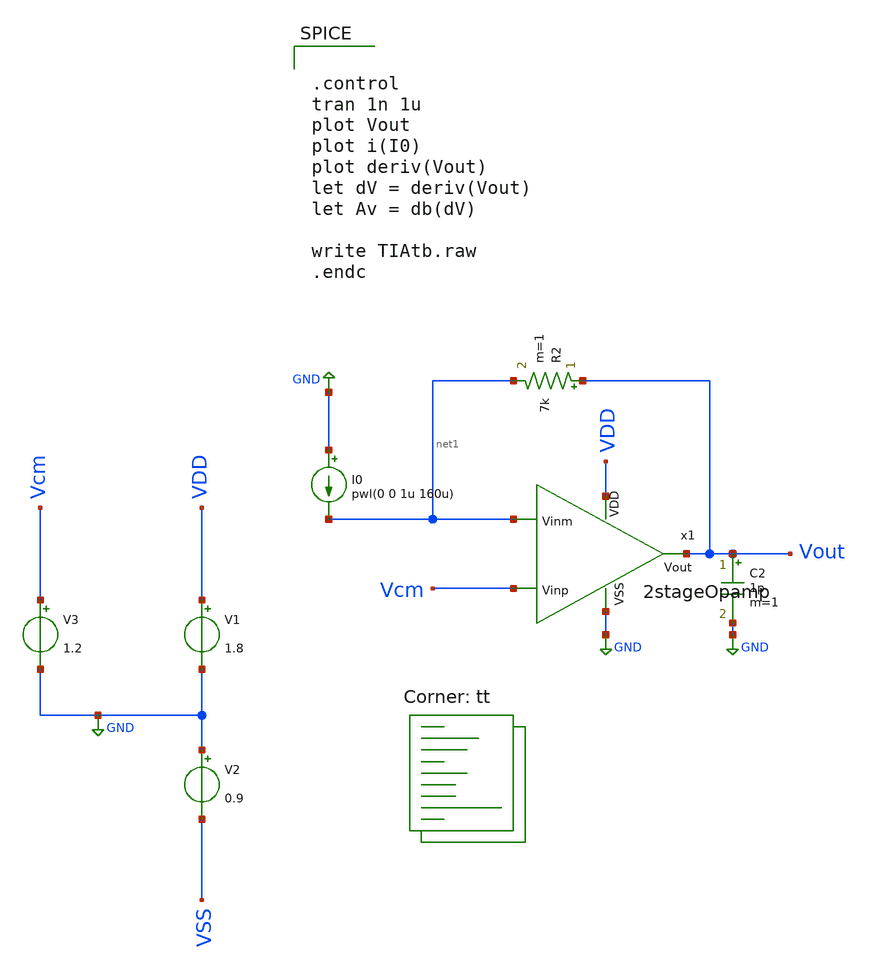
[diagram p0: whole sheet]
** sch_path: xschem/TestBenches/TIAtb.sch
**.subckt TIAtb
C2 Vout GND 1p m=1
x1 VDD net1 Vcm Vout GND 2stageOpamp
V1 VDD GND 1.8
V2 GND VSS 0.9
V3 Vcm GND 1.2
R2 Vout net1 7k m=1
I0 GND net1 pwl(0 0 1u 160u)
**** begin user architecture code


.control
tran 1n 1u
plot Vout
plot i(I0)
plot deriv(Vout)
let dV = deriv(Vout)
let Av = db(dV)

write TIAtb.raw
.endc



.lib $::SKYWATER_MODELS/sky130.lib.spice tt
**** end user architecture code
**.ends
.GLOBAL GND
.end
